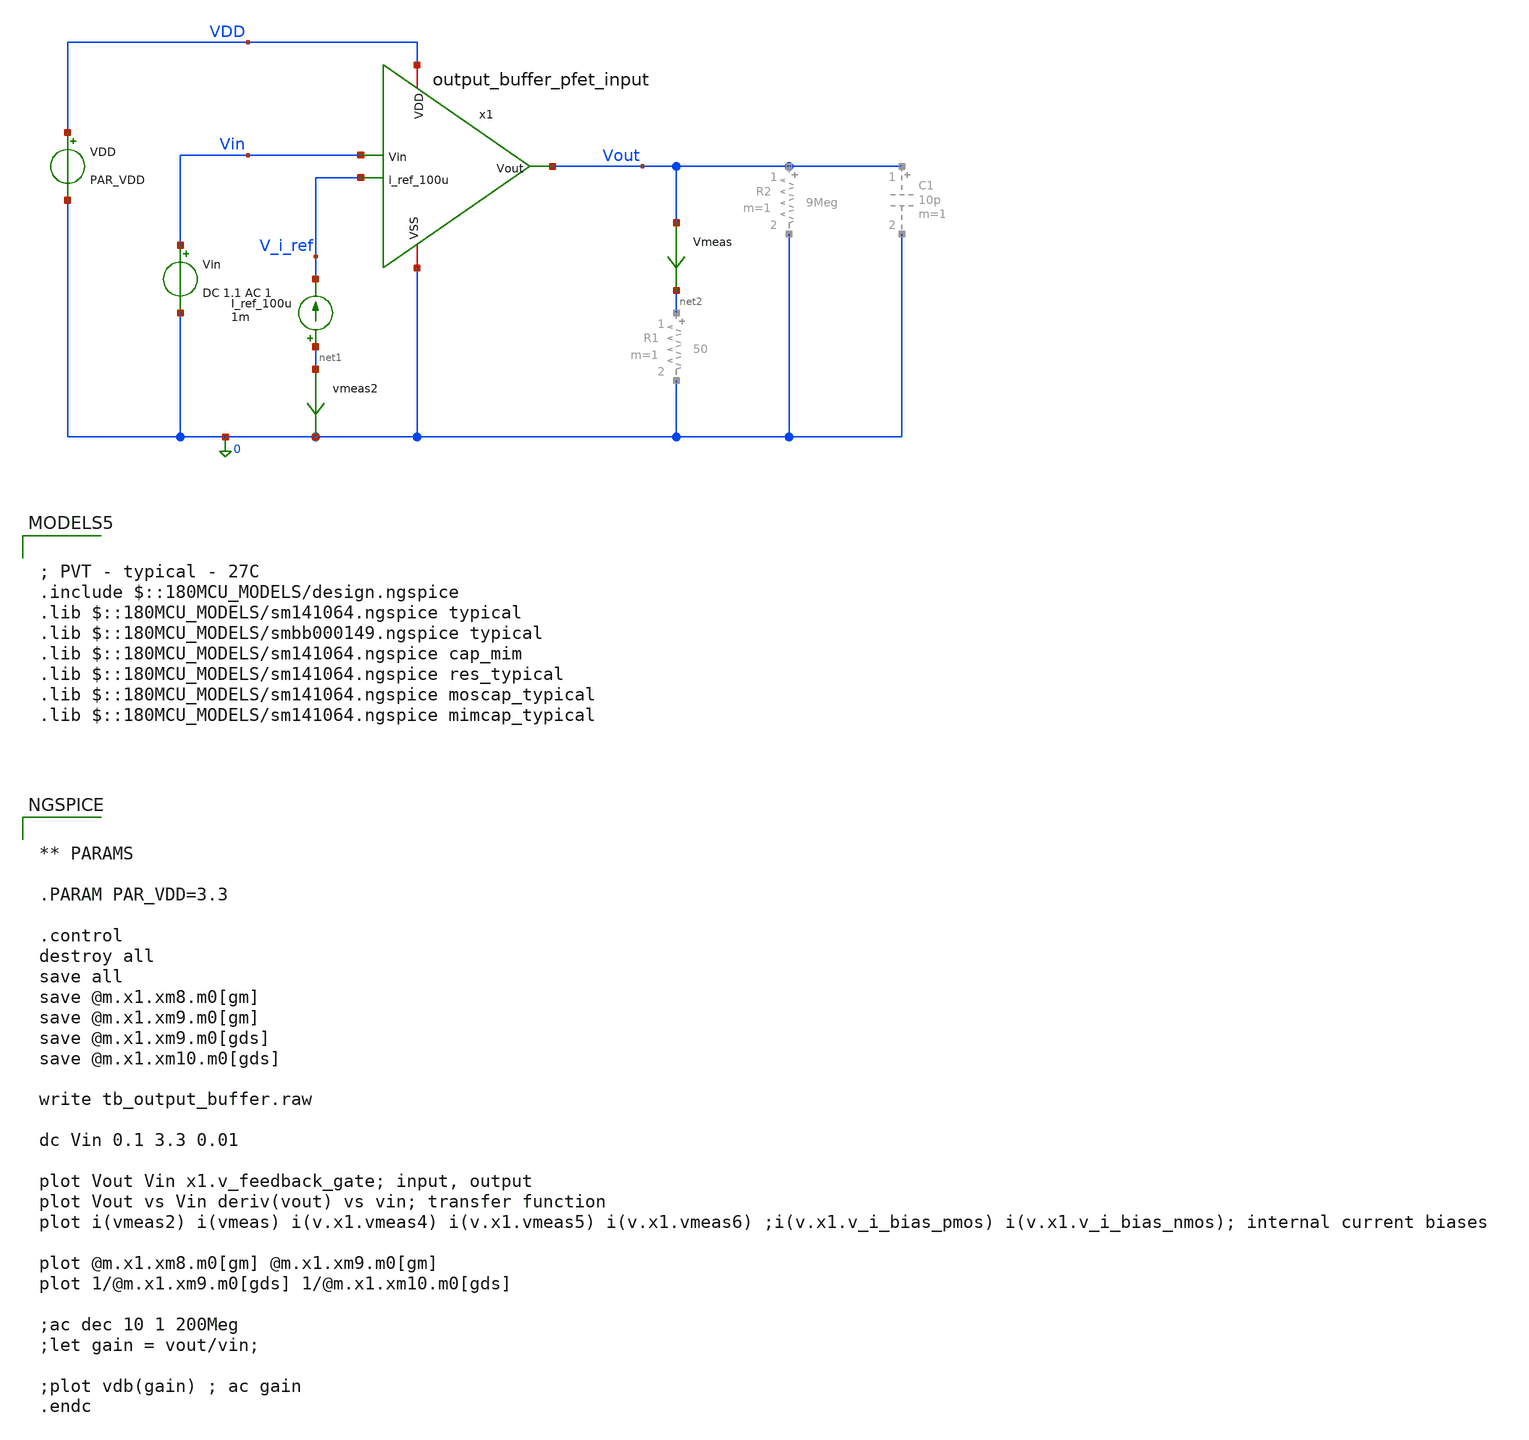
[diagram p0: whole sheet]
** sch_path: designs/output_buffer/testbench/tb_output_buffer_pfet_input.sch
**.subckt tb_output_buffer_pfet_input
I_ref_100u net1 V_i_ref 1m
Vin Vin 0 DC 1.1 AC 1
VDD VDD 0 PAR_VDD
vmeas2 net1 0 0
.save i(vmeas2)
x1 Vout Vin V_i_ref VDD 0 output_buffer_pfet_input
Vmeas Vout net2 0
.save i(vmeas)
**** begin user architecture code

; PVT - typical - 27C
.include $::180MCU_MODELS/design.ngspice
.lib $::180MCU_MODELS/sm141064.ngspice typical
.lib $::180MCU_MODELS/smbb000149.ngspice typical
.lib $::180MCU_MODELS/sm141064.ngspice cap_mim
.lib $::180MCU_MODELS/sm141064.ngspice res_typical
.lib $::180MCU_MODELS/sm141064.ngspice moscap_typical
.lib $::180MCU_MODELS/sm141064.ngspice mimcap_typical



** PARAMS

.PARAM PAR_VDD=3.3

.control
destroy all
save all
save @m.x1.xm8.m0[gm]
save @m.x1.xm9.m0[gm]
save @m.x1.xm9.m0[gds]
save @m.x1.xm10.m0[gds]

write tb_output_buffer.raw

dc Vin 0.1 3.3 0.01

plot Vout Vin x1.v_feedback_gate; input, output
plot Vout vs Vin deriv(vout) vs vin; transfer function
plot i(vmeas2) i(vmeas) i(v.x1.vmeas4) i(v.x1.vmeas5) i(v.x1.vmeas6) ;i(v.x1.v_i_bias_pmos)
+ i(v.x1.v_i_bias_nmos); internal current biases

plot @m.x1.xm8.m0[gm] @m.x1.xm9.m0[gm]
plot 1/@m.x1.xm9.m0[gds] 1/@m.x1.xm10.m0[gds]

;ac dec 10 1 200Meg
;let gain = vout/vin;

;plot vdb(gain) ; ac gain
.endc


**** end user architecture code
**.ends
.end
